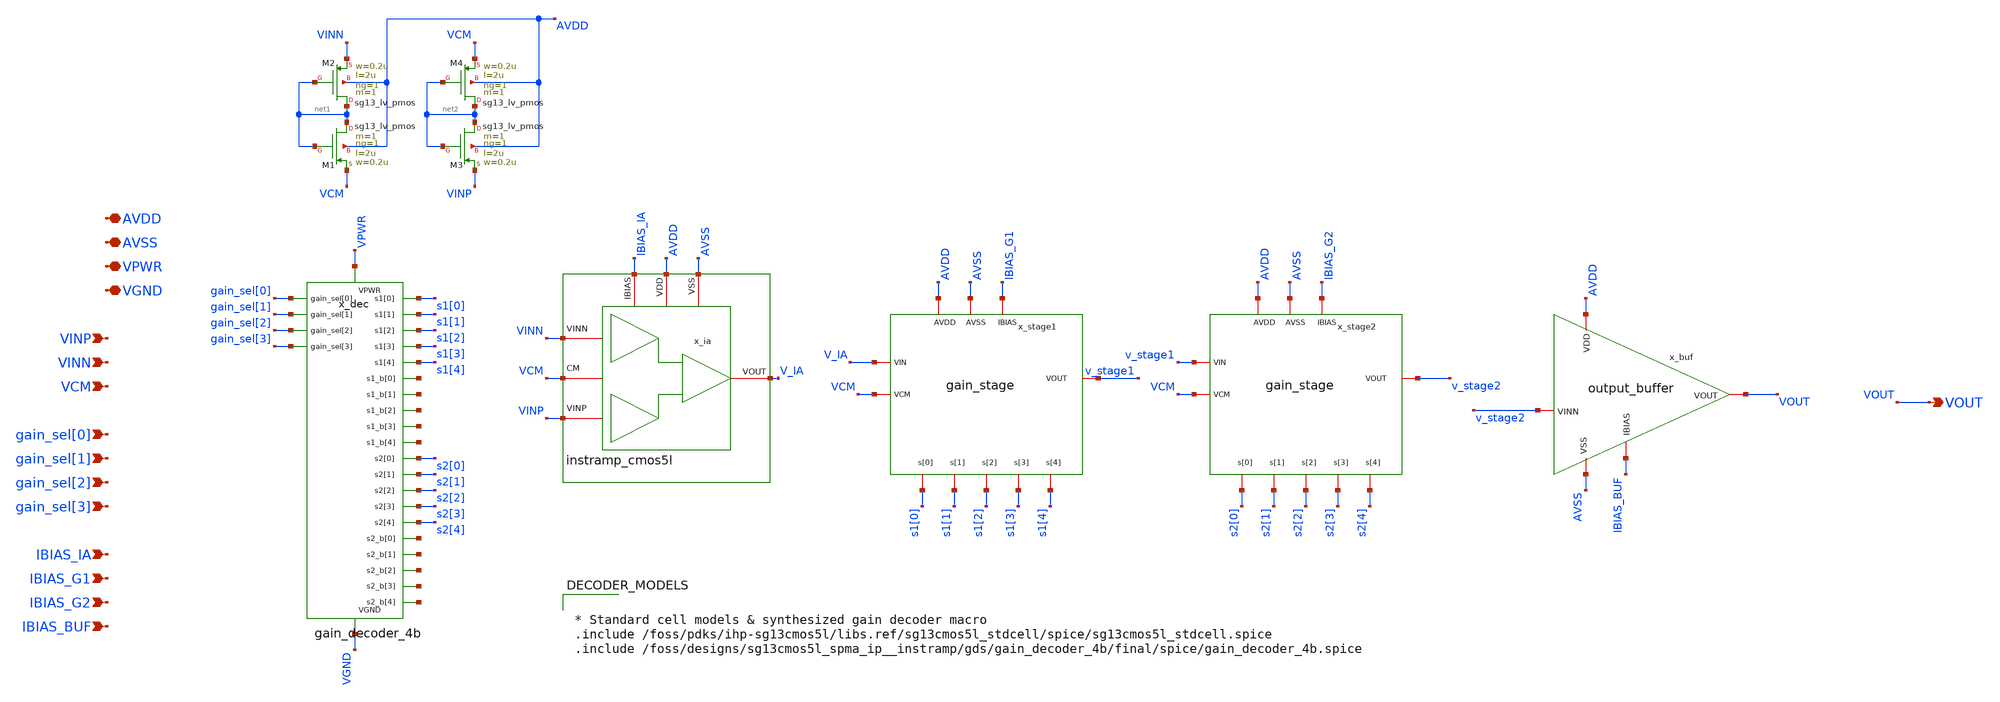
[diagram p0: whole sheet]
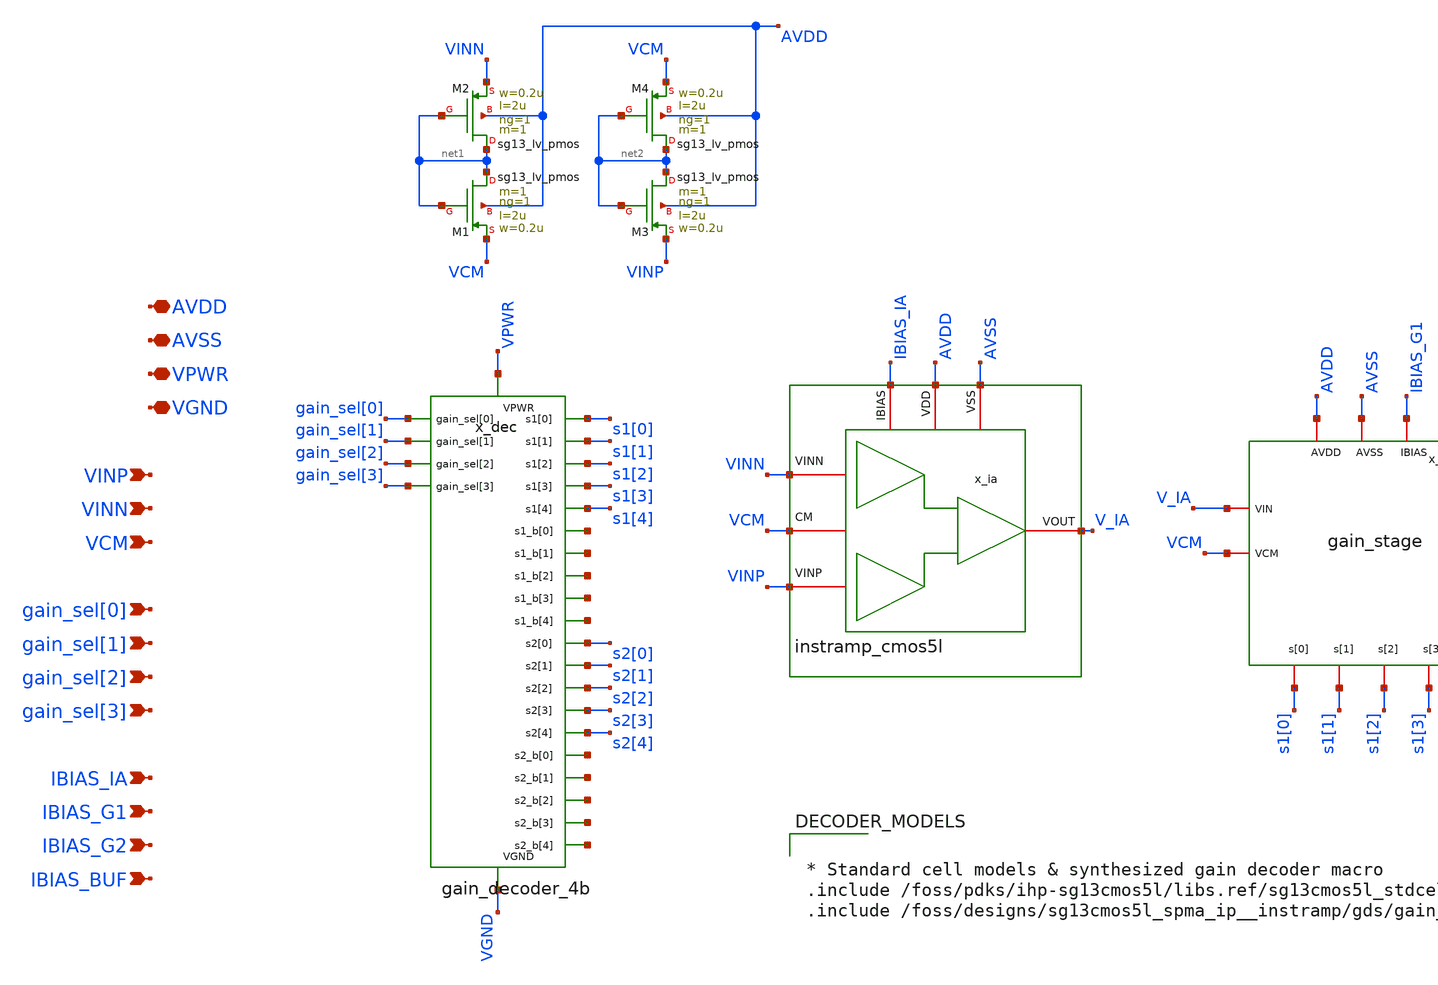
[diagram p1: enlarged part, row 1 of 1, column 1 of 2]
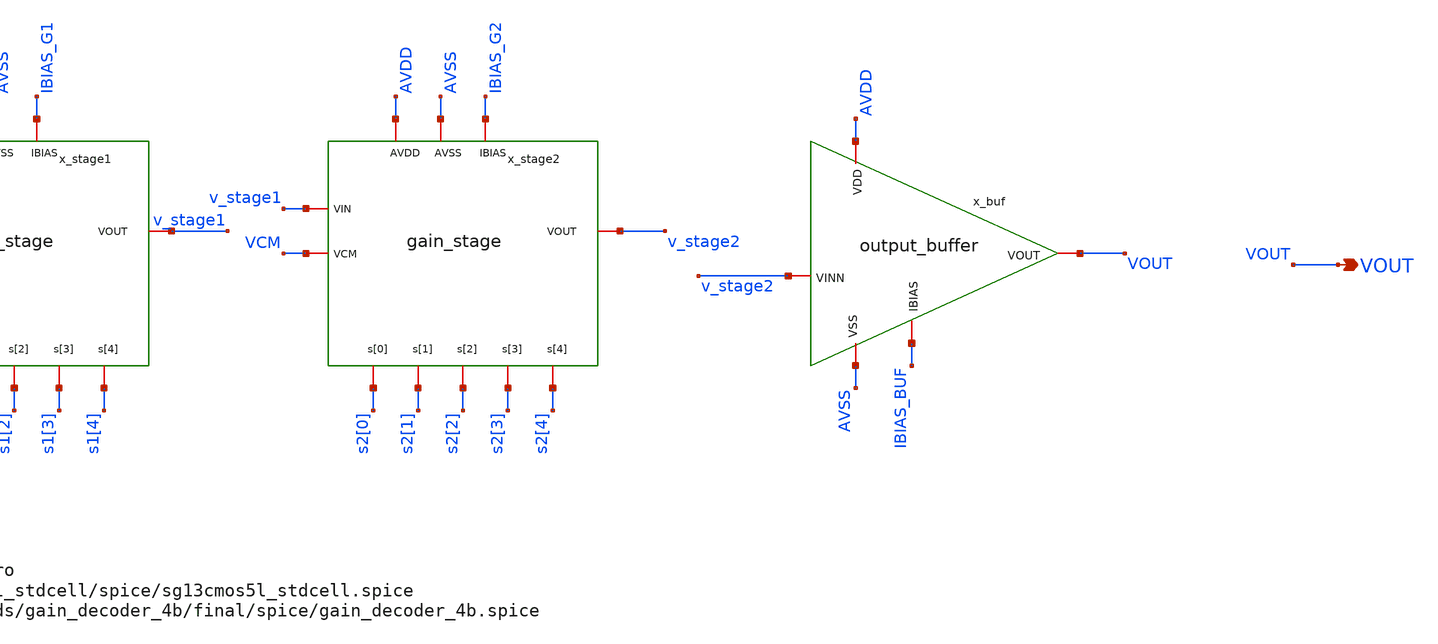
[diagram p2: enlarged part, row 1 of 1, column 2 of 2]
** sch_path: xschem/pgia_top/pgia_top.sch
**.subckt pgia_top AVDD AVSS VPWR VGND VINP VINN VCM gain_sel[0] gain_sel[1] gain_sel[2] gain_sel[3]
*+ IBIAS_IA IBIAS_G1 IBIAS_G2 IBIAS_BUF VOUT
*.iopin AVDD
*.iopin AVSS
*.iopin VPWR
*.iopin VGND
*.ipin VINP
*.ipin VINN
*.ipin VCM
*.ipin gain_sel[0]
*.ipin gain_sel[1]
*.ipin gain_sel[2]
*.ipin gain_sel[3]
*.ipin IBIAS_IA
*.ipin IBIAS_G1
*.ipin IBIAS_G2
*.ipin IBIAS_BUF
*.opin VOUT
x_dec VGND VPWR gain_sel[0] gain_sel[1] gain_sel[2] gain_sel[3] s1[0] s1[1] s1[2] s1[3] s1[4] net3
+ net4 net5 net6 net7 s2[0] s2[1] s2[2] s2[3] s2[4] net8 net9 net10 net11 net12 gain_decoder_4b
x_ia AVSS AVDD IBIAS_IA VINN V_IA VINP VCM instramp_cmos5l
x_stage1 AVDD AVSS IBIAS_G1 V_IA VCM v_stage1 s1[0] s1[1] s1[2] s1[3] s1[4] gain_stage
x_stage2 AVDD AVSS IBIAS_G2 v_stage1 VCM v_stage2 s2[0] s2[1] s2[2] s2[3] s2[4] gain_stage
x_buf AVDD AVSS IBIAS_BUF v_stage2 VOUT output_buffer
XM1 net1 net1 VCM AVDD sg13_lv_pmos w=0.2u l=2u ng=1 m=1 mm_ok=1
XM2 net1 net1 VINN AVDD sg13_lv_pmos w=0.2u l=2u ng=1 m=1 mm_ok=1
XM3 net2 net2 VINP AVDD sg13_lv_pmos w=0.2u l=2u ng=1 m=1 mm_ok=1
XM4 net2 net2 VCM AVDD sg13_lv_pmos w=0.2u l=2u ng=1 m=1 mm_ok=1
**** begin user architecture code


* Standard cell models & synthesized gain decoder macro
.include /foss/pdks/ihp-sg13cmos5l/libs.ref/sg13cmos5l_stdcell/spice/sg13cmos5l_stdcell.spice
.include /foss/designs/sg13cmos5l_spma_ip__instramp/gds/gain_decoder_4b/final/spice/gain_decoder_4b.spice


**** end user architecture code
**.ends
.end
